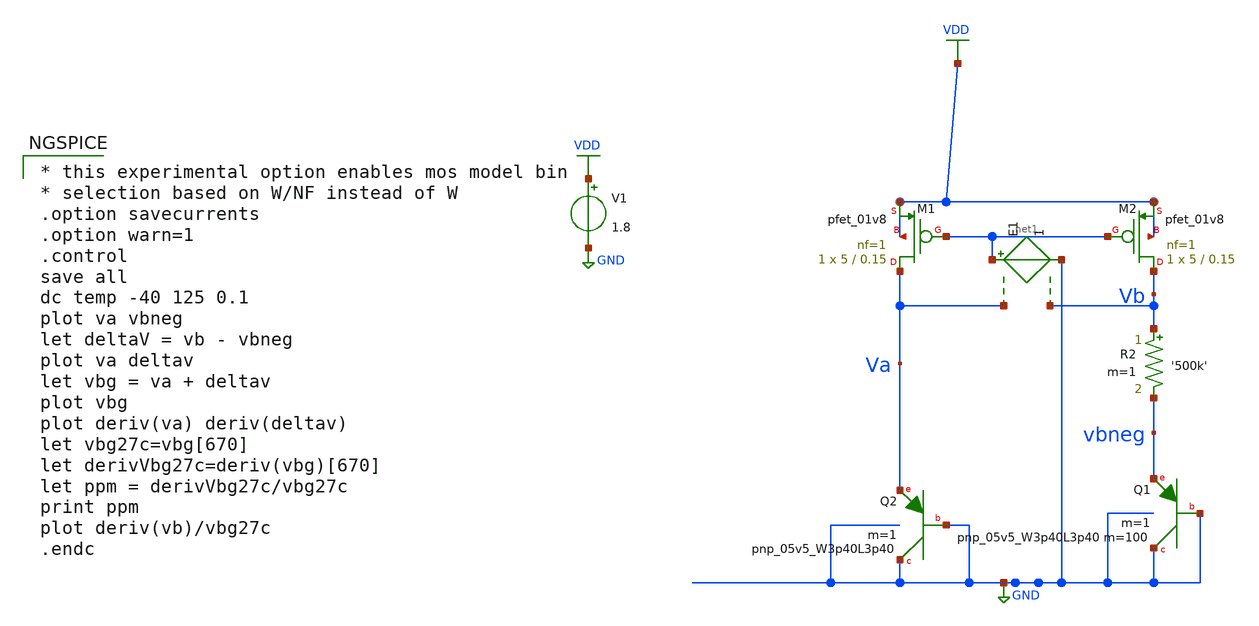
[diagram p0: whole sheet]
** sch_path: legacy/schematics/delta_vbe_ex.sch
**.subckt delta_vbe_ex
XQ1 GND GND vbneg sky130_fd_pr__pnp_05v5_W3p40L3p40 m=100 m=1
R2 Vb vbneg '500k' m=1
XQ2 GND GND Va sky130_fd_pr__pnp_05v5_W3p40L3p40 m=1
V1 VDD GND 1.8
XM1 Va net1 VDD VDD sky130_fd_pr__pfet_01v8 L=0.15 W=5 nf=1 ad='int((nf+1)/2) * W/nf * 0.29' as='int((nf+2)/2) * W/nf * 0.29'
+ pd='2*int((nf+1)/2) * (W/nf + 0.29)' ps='2*int((nf+2)/2) * (W/nf + 0.29)' nrd='0.29 / W' nrs='0.29 / W'
+ sa=0 sb=0 sd=0 mult=1 m=1
XM2 Vb net1 VDD VDD sky130_fd_pr__pfet_01v8 L=0.15 W=5 nf=1 ad='int((nf+1)/2) * W/nf * 0.29' as='int((nf+2)/2) * W/nf * 0.29'
+ pd='2*int((nf+1)/2) * (W/nf + 0.29)' ps='2*int((nf+2)/2) * (W/nf + 0.29)' nrd='0.29 / W' nrs='0.29 / W'
+ sa=0 sb=0 sd=0 mult=1 m=1
E1 net1 GND Va Vb 1
**** begin user architecture code

.include $::SKYWATER_MODELS/cells/nfet_01v8/sky130_fd_pr__nfet_01v8__tt.corner.spice
.include $::SKYWATER_MODELS/cells/nfet_01v8_lvt/sky130_fd_pr__nfet_01v8_lvt__tt.corner.spice
.include $::SKYWATER_MODELS/cells/pfet_01v8/sky130_fd_pr__pfet_01v8__tt.corner.spice
.include $::SKYWATER_MODELS/cells/nfet_03v3_nvt/sky130_fd_pr__nfet_03v3_nvt__tt.corner.spice
.include $::SKYWATER_MODELS/cells/nfet_05v0_nvt/sky130_fd_pr__nfet_05v0_nvt__tt.corner.spice
.include $::SKYWATER_MODELS/cells/esd_nfet_01v8/sky130_fd_pr__esd_nfet_01v8__tt.corner.spice
.include $::SKYWATER_MODELS/cells/pfet_01v8_lvt/sky130_fd_pr__pfet_01v8_lvt__tt.corner.spice
.include $::SKYWATER_MODELS/cells/pfet_01v8_hvt/sky130_fd_pr__pfet_01v8_hvt__tt.corner.spice
.include $::SKYWATER_MODELS/cells/esd_pfet_g5v0d10v5/sky130_fd_pr__esd_pfet_g5v0d10v5__tt.corner.spice
.include $::SKYWATER_MODELS/cells/pfet_g5v0d10v5/sky130_fd_pr__pfet_g5v0d10v5__tt.corner.spice
.include $::SKYWATER_MODELS/cells/pfet_g5v0d16v0/sky130_fd_pr__pfet_g5v0d16v0__tt.corner.spice
.include $::SKYWATER_MODELS/cells/nfet_g5v0d10v5/sky130_fd_pr__nfet_g5v0d10v5__tt.corner.spice
.include $::SKYWATER_MODELS/cells/nfet_g5v0d16v0/sky130_fd_pr__nfet_g5v0d16v0__tt_discrete.corner.spice
.include $::SKYWATER_MODELS/cells/esd_nfet_g5v0d10v5/sky130_fd_pr__esd_nfet_g5v0d10v5__tt.corner.spice
.include $::SKYWATER_MODELS/models/corners/tt/nonfet.spice
* Mismatch parameters
.include $::SKYWATER_MODELS/cells/nfet_01v8/sky130_fd_pr__nfet_01v8__mismatch.corner.spice
.include $::SKYWATER_MODELS/cells/pfet_01v8/sky130_fd_pr__pfet_01v8__mismatch.corner.spice
.include $::SKYWATER_MODELS/cells/nfet_01v8_lvt/sky130_fd_pr__nfet_01v8_lvt__mismatch.corner.spice
.include $::SKYWATER_MODELS/cells/pfet_01v8_lvt/sky130_fd_pr__pfet_01v8_lvt__mismatch.corner.spice
.include $::SKYWATER_MODELS/cells/pfet_01v8_hvt/sky130_fd_pr__pfet_01v8_hvt__mismatch.corner.spice
.include $::SKYWATER_MODELS/cells/nfet_g5v0d10v5/sky130_fd_pr__nfet_g5v0d10v5__mismatch.corner.spice
.include $::SKYWATER_MODELS/cells/pfet_g5v0d10v5/sky130_fd_pr__pfet_g5v0d10v5__mismatch.corner.spice
.include $::SKYWATER_MODELS/cells/nfet_05v0_nvt/sky130_fd_pr__nfet_05v0_nvt__mismatch.corner.spice
.include $::SKYWATER_MODELS/cells/nfet_03v3_nvt/sky130_fd_pr__nfet_03v3_nvt__mismatch.corner.spice
* Resistor$::SKYWATER_MODELS/Capacitor
.include $::SKYWATER_MODELS/models/r+c/res_typical__cap_typical.spice
.include $::SKYWATER_MODELS/models/r+c/res_typical__cap_typical__lin.spice
* Special cells
.include $::SKYWATER_MODELS/models/corners/tt/specialized_cells.spice
* All models
.include $::SKYWATER_MODELS/models/all.spice
.include $::SKYWATER_MODELS/cells/pnp_05v5/sky130_fd_pr__pnp_05v5_W3p40L3p40.model.spice
* Corner
.include $::SKYWATER_MODELS/models/corners/tt/rf.spice


* this experimental option enables mos model bin
* selection based on W/NF instead of W
.option savecurrents
.option warn=1
.control
save all
dc temp -40 125 0.1
plot va vbneg
let deltaV = vb - vbneg
plot va deltav
let vbg = va + deltav
plot vbg
plot deriv(va) deriv(deltav)
let vbg27c=vbg[670]
let derivVbg27c=deriv(vbg)[670]
let ppm = derivVbg27c/vbg27c
print ppm
plot deriv(vb)/vbg27c
.endc


**** end user architecture code
**.ends
.GLOBAL GND
.GLOBAL VDD
.end
